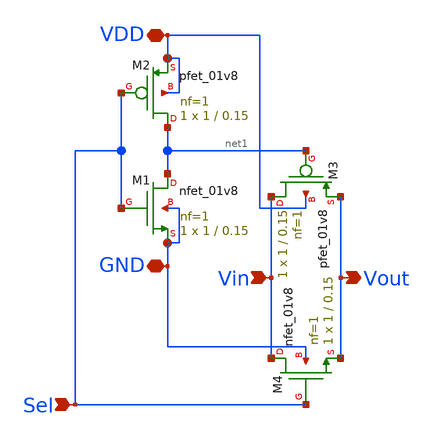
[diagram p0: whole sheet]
** sch_path: switch/open_switch.sch
**.subckt open_switch VDD GND Sel Vin Vout
*.iopin VDD
*.iopin GND
*.ipin Sel
*.ipin Vin
*.opin Vout
XM1 net1 Sel GND GND sky130_fd_pr__nfet_01v8 L=0.15 W=1 nf=1 ad='int((nf+1)/2) * W/nf * 0.29' as='int((nf+2)/2) * W/nf * 0.29'
+ pd='2*int((nf+1)/2) * (W/nf + 0.29)' ps='2*int((nf+2)/2) * (W/nf + 0.29)' nrd='0.29 / W' nrs='0.29 / W'
+ sa=0 sb=0 sd=0 mult=1 m=1
XM2 net1 Sel VDD VDD sky130_fd_pr__pfet_01v8 L=0.15 W=1 nf=1 ad='int((nf+1)/2) * W/nf * 0.29' as='int((nf+2)/2) * W/nf * 0.29'
+ pd='2*int((nf+1)/2) * (W/nf + 0.29)' ps='2*int((nf+2)/2) * (W/nf + 0.29)' nrd='0.29 / W' nrs='0.29 / W'
+ sa=0 sb=0 sd=0 mult=1 m=1
XM3 Vin net1 Vout VDD sky130_fd_pr__pfet_01v8 L=0.15 W=1 nf=1 ad='int((nf+1)/2) * W/nf * 0.29' as='int((nf+2)/2) * W/nf * 0.29'
+ pd='2*int((nf+1)/2) * (W/nf + 0.29)' ps='2*int((nf+2)/2) * (W/nf + 0.29)' nrd='0.29 / W' nrs='0.29 / W'
+ sa=0 sb=0 sd=0 mult=1 m=1
XM4 Vin Sel Vout GND sky130_fd_pr__nfet_01v8 L=0.15 W=1 nf=1 ad='int((nf+1)/2) * W/nf * 0.29' as='int((nf+2)/2) * W/nf * 0.29'
+ pd='2*int((nf+1)/2) * (W/nf + 0.29)' ps='2*int((nf+2)/2) * (W/nf + 0.29)' nrd='0.29 / W' nrs='0.29 / W'
+ sa=0 sb=0 sd=0 mult=1 m=1
**.ends
.end
